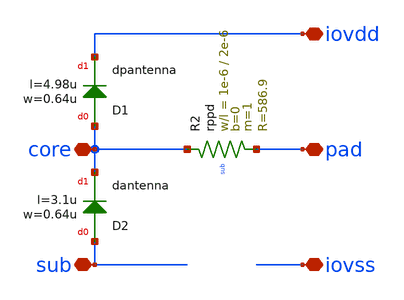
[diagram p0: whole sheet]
** sch_path: ihp-sg13g2/sg13g2_io/xschem/sg13g2_SecondaryProtection_noptap.sch
**.subckt sg13g2_SecondaryProtection_noptap iovss core pad iovdd sub
*.iopin iovss
*.iopin core
*.iopin pad
*.iopin iovdd
*.iopin sub
XD1 core iovdd dpantenna l=4.98u w=0.64u
XR2 core pad sub rppd w=1e-6 l=2e-6 m=1 b=0 mm_ok=1
XD2 sub core dantenna l=3.1u w=0.64u
**.ends
.end
